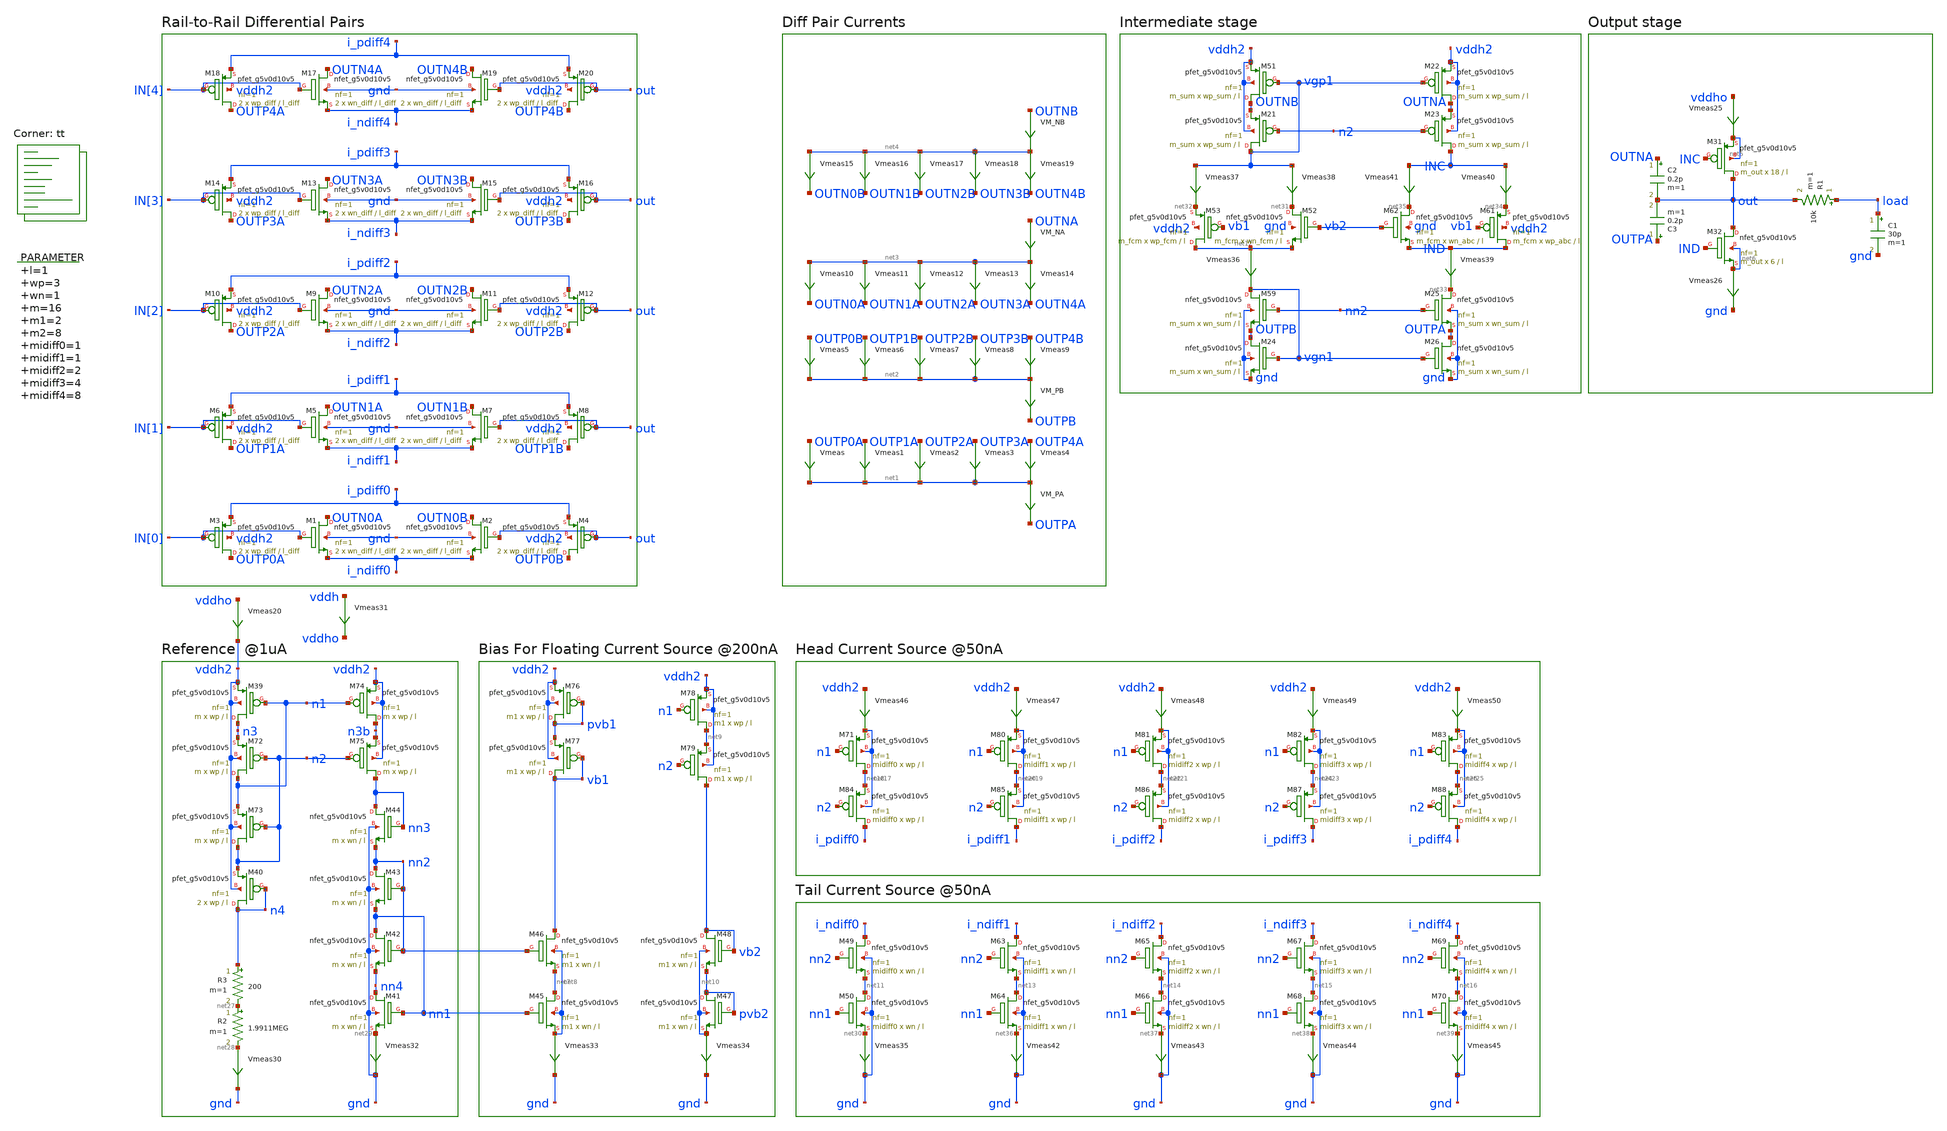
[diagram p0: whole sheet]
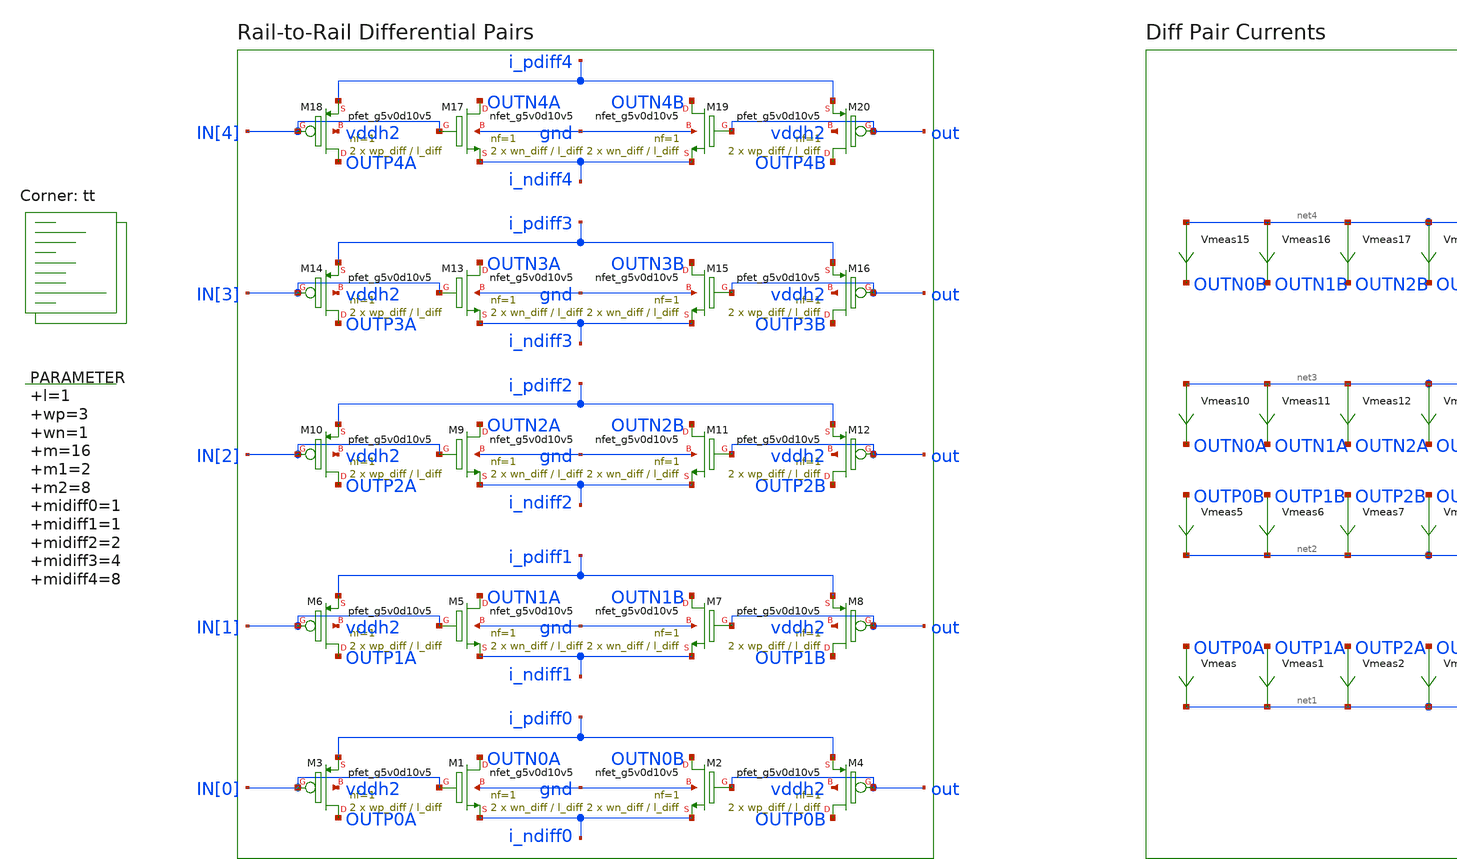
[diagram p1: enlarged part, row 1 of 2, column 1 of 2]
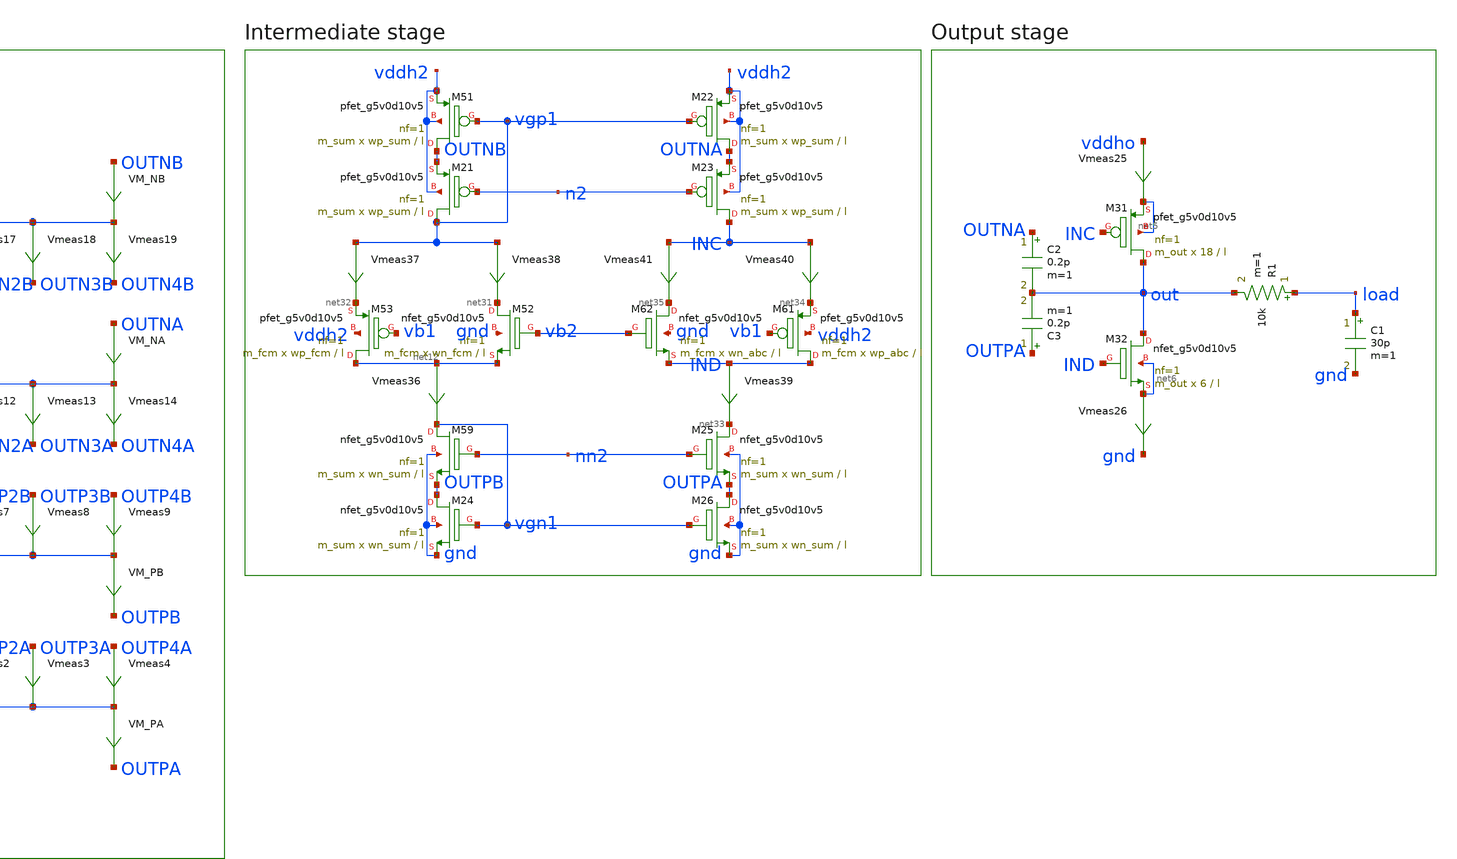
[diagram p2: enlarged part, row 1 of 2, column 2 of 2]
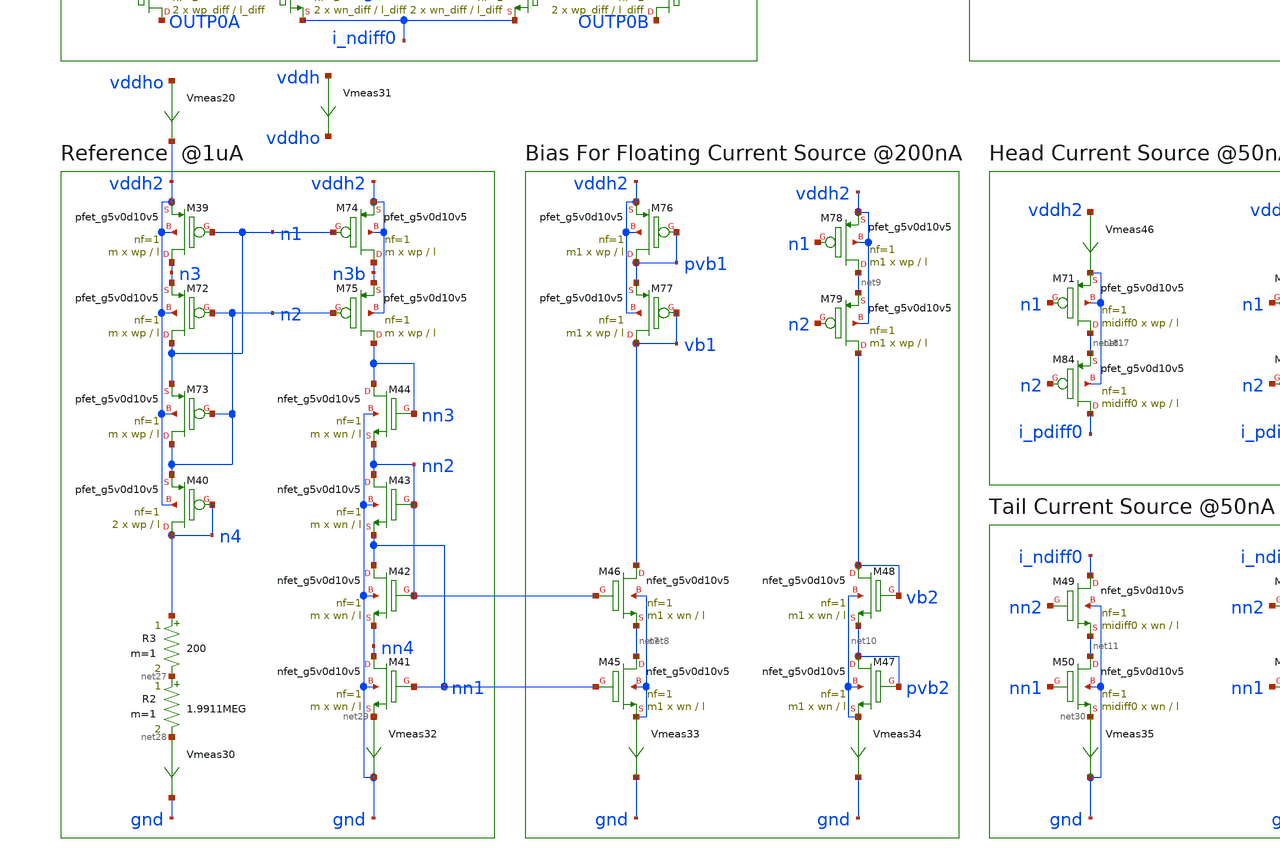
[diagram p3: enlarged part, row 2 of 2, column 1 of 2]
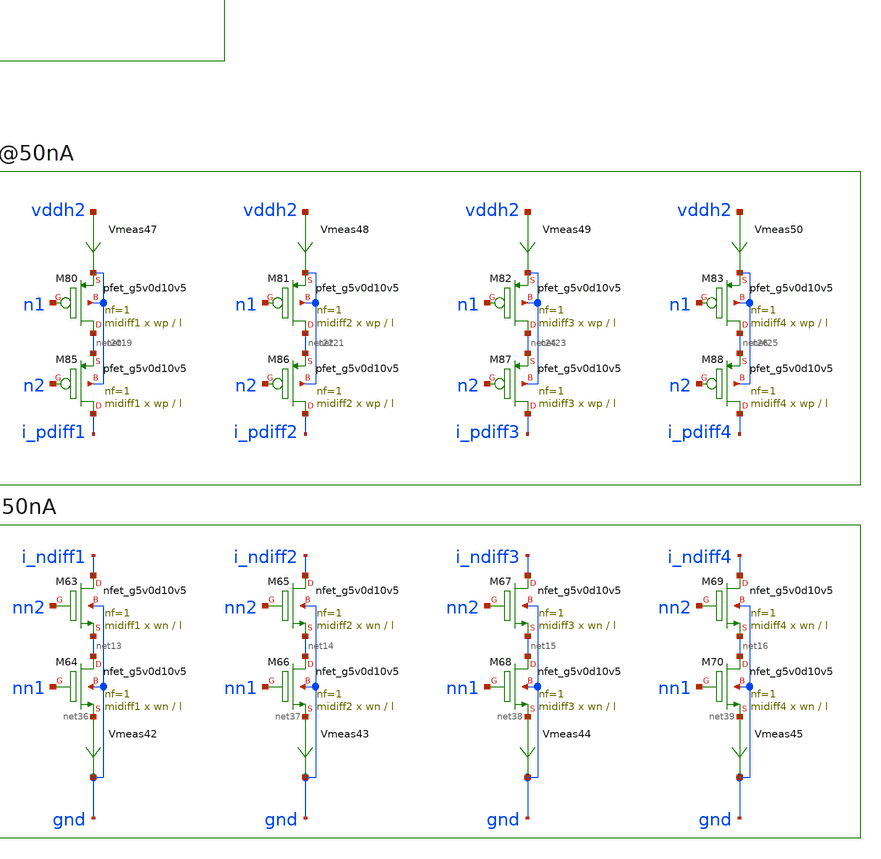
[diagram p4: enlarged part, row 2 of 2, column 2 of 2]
** sch_path: xschem/op_amp_v2-tb.sch
**.subckt op_amp_v2-tb
XM1 OUTN0A IN[0] i_ndiff0 gnd sky130_fd_pr__nfet_g5v0d10v5 L=l_diff W=wn_diff nf=1 ad='int((nf+1)/2) * W/nf * 0.29'
+ as='int((nf+2)/2) * W/nf * 0.29' pd='2*int((nf+1)/2) * (W/nf + 0.29)' ps='2*int((nf+2)/2) * (W/nf + 0.29)'
+ nrd='0.29 / W' nrs='0.29 / W' sa=0 sb=0 sd=0 mult=2 m=2
XM3 OUTP0A IN[0] i_pdiff0 vddh2 sky130_fd_pr__pfet_g5v0d10v5 L=l_diff W=wp_diff nf=1 ad='int((nf+1)/2) * W/nf * 0.29'
+ as='int((nf+2)/2) * W/nf * 0.29' pd='2*int((nf+1)/2) * (W/nf + 0.29)' ps='2*int((nf+2)/2) * (W/nf + 0.29)'
+ nrd='0.29 / W' nrs='0.29 / W' sa=0 sb=0 sd=0 mult=2 m=2
Vmeas OUTP0A net1 0
.save i(vmeas)
Vmeas1 OUTP1A net1 0
.save i(vmeas1)
Vmeas2 OUTP2A net1 0
.save i(vmeas2)
Vmeas3 OUTP3A net1 0
.save i(vmeas3)
Vmeas4 OUTP4A net1 0
.save i(vmeas4)
Vmeas5 OUTP0B net2 0
.save i(vmeas5)
Vmeas6 OUTP1B net2 0
.save i(vmeas6)
Vmeas7 OUTP2B net2 0
.save i(vmeas7)
Vmeas8 OUTP3B net2 0
.save i(vmeas8)
Vmeas9 OUTP4B net2 0
.save i(vmeas9)
Vmeas10 net3 OUTN0A 0
.save i(vmeas10)
Vmeas11 net3 OUTN1A 0
.save i(vmeas11)
Vmeas12 net3 OUTN2A 0
.save i(vmeas12)
Vmeas13 net3 OUTN3A 0
.save i(vmeas13)
Vmeas14 net3 OUTN4A 0
.save i(vmeas14)
Vmeas15 net4 OUTN0B 0
.save i(vmeas15)
Vmeas16 net4 OUTN1B 0
.save i(vmeas16)
Vmeas17 net4 OUTN2B 0
.save i(vmeas17)
Vmeas18 net4 OUTN3B 0
.save i(vmeas18)
Vmeas19 net4 OUTN4B 0
.save i(vmeas19)
XM31 out INC net5 net5 sky130_fd_pr__pfet_g5v0d10v5 L=l W=18 nf=1 ad='int((nf+1)/2) * W/nf * 0.29' as='int((nf+2)/2) * W/nf * 0.29'
+ pd='2*int((nf+1)/2) * (W/nf + 0.29)' ps='2*int((nf+2)/2) * (W/nf + 0.29)' nrd='0.29 / W' nrs='0.29 / W'
+ sa=0 sb=0 sd=0 mult=m_out m=m_out
XM32 out IND net6 net6 sky130_fd_pr__nfet_g5v0d10v5 L=l W=6 nf=1 ad='int((nf+1)/2) * W/nf * 0.29' as='int((nf+2)/2) * W/nf * 0.29'
+ pd='2*int((nf+1)/2) * (W/nf + 0.29)' ps='2*int((nf+2)/2) * (W/nf + 0.29)' nrd='0.29 / W' nrs='0.29 / W'
+ sa=0 sb=0 sd=0 mult=m_out m=m_out
R1 load out 10k m=1
Vmeas25 vddho net5 0
.save i(vmeas25)
Vmeas26 net6 gnd 0
.save i(vmeas26)
C1 load gnd 30p m=1
VM_NB OUTNB net4 0
.save i(vm_nb)
VM_NA OUTNA net3 0
.save i(vm_na)
VM_PB net2 OUTPB 0
.save i(vm_pb)
VM_PA net1 OUTPA 0
.save i(vm_pa)
C2 OUTNA out 0.2p m=1
C3 OUTPA out 0.2p m=1
XM2 OUTN0B out i_ndiff0 gnd sky130_fd_pr__nfet_g5v0d10v5 L=l_diff W=wn_diff nf=1 ad='int((nf+1)/2) * W/nf * 0.29'
+ as='int((nf+2)/2) * W/nf * 0.29' pd='2*int((nf+1)/2) * (W/nf + 0.29)' ps='2*int((nf+2)/2) * (W/nf + 0.29)'
+ nrd='0.29 / W' nrs='0.29 / W' sa=0 sb=0 sd=0 mult=2 m=2
XM4 OUTP0B out i_pdiff0 vddh2 sky130_fd_pr__pfet_g5v0d10v5 L=l_diff W=wp_diff nf=1 ad='int((nf+1)/2) * W/nf * 0.29'
+ as='int((nf+2)/2) * W/nf * 0.29' pd='2*int((nf+1)/2) * (W/nf + 0.29)' ps='2*int((nf+2)/2) * (W/nf + 0.29)'
+ nrd='0.29 / W' nrs='0.29 / W' sa=0 sb=0 sd=0 mult=2 m=2
XM5 OUTN1A IN[1] i_ndiff1 gnd sky130_fd_pr__nfet_g5v0d10v5 L=l_diff W=wn_diff nf=1 ad='int((nf+1)/2) * W/nf * 0.29'
+ as='int((nf+2)/2) * W/nf * 0.29' pd='2*int((nf+1)/2) * (W/nf + 0.29)' ps='2*int((nf+2)/2) * (W/nf + 0.29)'
+ nrd='0.29 / W' nrs='0.29 / W' sa=0 sb=0 sd=0 mult=2 m=2
XM6 OUTP1A IN[1] i_pdiff1 vddh2 sky130_fd_pr__pfet_g5v0d10v5 L=l_diff W=wp_diff nf=1 ad='int((nf+1)/2) * W/nf * 0.29'
+ as='int((nf+2)/2) * W/nf * 0.29' pd='2*int((nf+1)/2) * (W/nf + 0.29)' ps='2*int((nf+2)/2) * (W/nf + 0.29)'
+ nrd='0.29 / W' nrs='0.29 / W' sa=0 sb=0 sd=0 mult=2 m=2
XM7 OUTN1B out i_ndiff1 gnd sky130_fd_pr__nfet_g5v0d10v5 L=l_diff W=wn_diff nf=1 ad='int((nf+1)/2) * W/nf * 0.29'
+ as='int((nf+2)/2) * W/nf * 0.29' pd='2*int((nf+1)/2) * (W/nf + 0.29)' ps='2*int((nf+2)/2) * (W/nf + 0.29)'
+ nrd='0.29 / W' nrs='0.29 / W' sa=0 sb=0 sd=0 mult=2 m=2
XM8 OUTP1B out i_pdiff1 vddh2 sky130_fd_pr__pfet_g5v0d10v5 L=l_diff W=wp_diff nf=1 ad='int((nf+1)/2) * W/nf * 0.29'
+ as='int((nf+2)/2) * W/nf * 0.29' pd='2*int((nf+1)/2) * (W/nf + 0.29)' ps='2*int((nf+2)/2) * (W/nf + 0.29)'
+ nrd='0.29 / W' nrs='0.29 / W' sa=0 sb=0 sd=0 mult=2 m=2
XM9 OUTN2A IN[2] i_ndiff2 gnd sky130_fd_pr__nfet_g5v0d10v5 L=l_diff W=wn_diff nf=1 ad='int((nf+1)/2) * W/nf * 0.29'
+ as='int((nf+2)/2) * W/nf * 0.29' pd='2*int((nf+1)/2) * (W/nf + 0.29)' ps='2*int((nf+2)/2) * (W/nf + 0.29)'
+ nrd='0.29 / W' nrs='0.29 / W' sa=0 sb=0 sd=0 mult=2 m=2
XM10 OUTP2A IN[2] i_pdiff2 vddh2 sky130_fd_pr__pfet_g5v0d10v5 L=l_diff W=wp_diff nf=1 ad='int((nf+1)/2) * W/nf * 0.29'
+ as='int((nf+2)/2) * W/nf * 0.29' pd='2*int((nf+1)/2) * (W/nf + 0.29)' ps='2*int((nf+2)/2) * (W/nf + 0.29)'
+ nrd='0.29 / W' nrs='0.29 / W' sa=0 sb=0 sd=0 mult=2 m=2
XM11 OUTN2B out i_ndiff2 gnd sky130_fd_pr__nfet_g5v0d10v5 L=l_diff W=wn_diff nf=1 ad='int((nf+1)/2) * W/nf * 0.29'
+ as='int((nf+2)/2) * W/nf * 0.29' pd='2*int((nf+1)/2) * (W/nf + 0.29)' ps='2*int((nf+2)/2) * (W/nf + 0.29)'
+ nrd='0.29 / W' nrs='0.29 / W' sa=0 sb=0 sd=0 mult=2 m=2
XM12 OUTP2B out i_pdiff2 vddh2 sky130_fd_pr__pfet_g5v0d10v5 L=l_diff W=wp_diff nf=1 ad='int((nf+1)/2) * W/nf * 0.29'
+ as='int((nf+2)/2) * W/nf * 0.29' pd='2*int((nf+1)/2) * (W/nf + 0.29)' ps='2*int((nf+2)/2) * (W/nf + 0.29)'
+ nrd='0.29 / W' nrs='0.29 / W' sa=0 sb=0 sd=0 mult=2 m=2
XM13 OUTN3A IN[3] i_ndiff3 gnd sky130_fd_pr__nfet_g5v0d10v5 L=l_diff W=wn_diff nf=1 ad='int((nf+1)/2) * W/nf * 0.29'
+ as='int((nf+2)/2) * W/nf * 0.29' pd='2*int((nf+1)/2) * (W/nf + 0.29)' ps='2*int((nf+2)/2) * (W/nf + 0.29)'
+ nrd='0.29 / W' nrs='0.29 / W' sa=0 sb=0 sd=0 mult=2 m=2
XM14 OUTP3A IN[3] i_pdiff3 vddh2 sky130_fd_pr__pfet_g5v0d10v5 L=l_diff W=wp_diff nf=1 ad='int((nf+1)/2) * W/nf * 0.29'
+ as='int((nf+2)/2) * W/nf * 0.29' pd='2*int((nf+1)/2) * (W/nf + 0.29)' ps='2*int((nf+2)/2) * (W/nf + 0.29)'
+ nrd='0.29 / W' nrs='0.29 / W' sa=0 sb=0 sd=0 mult=2 m=2
XM15 OUTN3B out i_ndiff3 gnd sky130_fd_pr__nfet_g5v0d10v5 L=l_diff W=wn_diff nf=1 ad='int((nf+1)/2) * W/nf * 0.29'
+ as='int((nf+2)/2) * W/nf * 0.29' pd='2*int((nf+1)/2) * (W/nf + 0.29)' ps='2*int((nf+2)/2) * (W/nf + 0.29)'
+ nrd='0.29 / W' nrs='0.29 / W' sa=0 sb=0 sd=0 mult=2 m=2
XM16 OUTP3B out i_pdiff3 vddh2 sky130_fd_pr__pfet_g5v0d10v5 L=l_diff W=wp_diff nf=1 ad='int((nf+1)/2) * W/nf * 0.29'
+ as='int((nf+2)/2) * W/nf * 0.29' pd='2*int((nf+1)/2) * (W/nf + 0.29)' ps='2*int((nf+2)/2) * (W/nf + 0.29)'
+ nrd='0.29 / W' nrs='0.29 / W' sa=0 sb=0 sd=0 mult=2 m=2
XM17 OUTN4A IN[4] i_ndiff4 gnd sky130_fd_pr__nfet_g5v0d10v5 L=l_diff W=wn_diff nf=1 ad='int((nf+1)/2) * W/nf * 0.29'
+ as='int((nf+2)/2) * W/nf * 0.29' pd='2*int((nf+1)/2) * (W/nf + 0.29)' ps='2*int((nf+2)/2) * (W/nf + 0.29)'
+ nrd='0.29 / W' nrs='0.29 / W' sa=0 sb=0 sd=0 mult=2 m=2
XM18 OUTP4A IN[4] i_pdiff4 vddh2 sky130_fd_pr__pfet_g5v0d10v5 L=l_diff W=wp_diff nf=1 ad='int((nf+1)/2) * W/nf * 0.29'
+ as='int((nf+2)/2) * W/nf * 0.29' pd='2*int((nf+1)/2) * (W/nf + 0.29)' ps='2*int((nf+2)/2) * (W/nf + 0.29)'
+ nrd='0.29 / W' nrs='0.29 / W' sa=0 sb=0 sd=0 mult=2 m=2
XM19 OUTN4B out i_ndiff4 gnd sky130_fd_pr__nfet_g5v0d10v5 L=l_diff W=wn_diff nf=1 ad='int((nf+1)/2) * W/nf * 0.29'
+ as='int((nf+2)/2) * W/nf * 0.29' pd='2*int((nf+1)/2) * (W/nf + 0.29)' ps='2*int((nf+2)/2) * (W/nf + 0.29)'
+ nrd='0.29 / W' nrs='0.29 / W' sa=0 sb=0 sd=0 mult=2 m=2
XM20 OUTP4B out i_pdiff4 vddh2 sky130_fd_pr__pfet_g5v0d10v5 L=l_diff W=wp_diff nf=1 ad='int((nf+1)/2) * W/nf * 0.29'
+ as='int((nf+2)/2) * W/nf * 0.29' pd='2*int((nf+1)/2) * (W/nf + 0.29)' ps='2*int((nf+2)/2) * (W/nf + 0.29)'
+ nrd='0.29 / W' nrs='0.29 / W' sa=0 sb=0 sd=0 mult=2 m=2
XM39 n3 n1 vddh2 vddh2 sky130_fd_pr__pfet_g5v0d10v5 L=l W=wp nf=1 ad='int((nf+1)/2) * W/nf * 0.29' as='int((nf+2)/2) * W/nf * 0.29'
+ pd='2*int((nf+1)/2) * (W/nf + 0.29)' ps='2*int((nf+2)/2) * (W/nf + 0.29)' nrd='0.29 / W' nrs='0.29 / W'
+ sa=0 sb=0 sd=0 mult=m m=m
R2 net27 net28 1.9911MEG m=1
Vmeas30 net28 gnd 0
.save i(vmeas30)
R3 n4 net27 200 m=1
XM40 n4 n4 n2 vddh2 sky130_fd_pr__pfet_g5v0d10v5 L=l W=wp nf=1 ad='int((nf+1)/2) * W/nf * 0.29' as='int((nf+2)/2) * W/nf * 0.29'
+ pd='2*int((nf+1)/2) * (W/nf + 0.29)' ps='2*int((nf+2)/2) * (W/nf + 0.29)' nrd='0.29 / W' nrs='0.29 / W'
+ sa=0 sb=0 sd=0 mult=2 m=2
Vmeas31 vddh vddho 0
.save i(vmeas31)
XM41 nn4 nn1 net29 gnd sky130_fd_pr__nfet_g5v0d10v5 L=l W=wn nf=1 ad='int((nf+1)/2) * W/nf * 0.29' as='int((nf+2)/2) * W/nf * 0.29'
+ pd='2*int((nf+1)/2) * (W/nf + 0.29)' ps='2*int((nf+2)/2) * (W/nf + 0.29)' nrd='0.29 / W' nrs='0.29 / W'
+ sa=0 sb=0 sd=0 mult=m m=m
XM42 nn1 nn2 nn4 gnd sky130_fd_pr__nfet_g5v0d10v5 L=l W=wn nf=1 ad='int((nf+1)/2) * W/nf * 0.29' as='int((nf+2)/2) * W/nf * 0.29'
+ pd='2*int((nf+1)/2) * (W/nf + 0.29)' ps='2*int((nf+2)/2) * (W/nf + 0.29)' nrd='0.29 / W' nrs='0.29 / W'
+ sa=0 sb=0 sd=0 mult=m m=m
XM43 nn2 nn2 nn1 gnd sky130_fd_pr__nfet_g5v0d10v5 L=l W=wn nf=1 ad='int((nf+1)/2) * W/nf * 0.29' as='int((nf+2)/2) * W/nf * 0.29'
+ pd='2*int((nf+1)/2) * (W/nf + 0.29)' ps='2*int((nf+2)/2) * (W/nf + 0.29)' nrd='0.29 / W' nrs='0.29 / W'
+ sa=0 sb=0 sd=0 mult=m m=m
XM44 nn3 nn3 nn2 gnd sky130_fd_pr__nfet_g5v0d10v5 L=l W=wn nf=1 ad='int((nf+1)/2) * W/nf * 0.29' as='int((nf+2)/2) * W/nf * 0.29'
+ pd='2*int((nf+1)/2) * (W/nf + 0.29)' ps='2*int((nf+2)/2) * (W/nf + 0.29)' nrd='0.29 / W' nrs='0.29 / W'
+ sa=0 sb=0 sd=0 mult=m m=m
Vmeas32 net29 gnd 0
.save i(vmeas32)
XM45 net7 nn1 net8 net8 sky130_fd_pr__nfet_g5v0d10v5 L=l W=wn nf=1 ad='int((nf+1)/2) * W/nf * 0.29' as='int((nf+2)/2) * W/nf * 0.29'
+ pd='2*int((nf+1)/2) * (W/nf + 0.29)' ps='2*int((nf+2)/2) * (W/nf + 0.29)' nrd='0.29 / W' nrs='0.29 / W'
+ sa=0 sb=0 sd=0 mult=m1 m=m1
XM46 vb1 nn2 net7 net8 sky130_fd_pr__nfet_g5v0d10v5 L=l W=wn nf=1 ad='int((nf+1)/2) * W/nf * 0.29' as='int((nf+2)/2) * W/nf * 0.29'
+ pd='2*int((nf+1)/2) * (W/nf + 0.29)' ps='2*int((nf+2)/2) * (W/nf + 0.29)' nrd='0.29 / W' nrs='0.29 / W'
+ sa=0 sb=0 sd=0 mult=m1 m=m1
Vmeas33 net8 gnd 0
.save i(vmeas33)
XM47 pvb2 pvb2 net10 net10 sky130_fd_pr__nfet_g5v0d10v5 L=l W=wn nf=1 ad='int((nf+1)/2) * W/nf * 0.29'
+ as='int((nf+2)/2) * W/nf * 0.29' pd='2*int((nf+1)/2) * (W/nf + 0.29)' ps='2*int((nf+2)/2) * (W/nf + 0.29)'
+ nrd='0.29 / W' nrs='0.29 / W' sa=0 sb=0 sd=0 mult=m1 m=m1
XM48 vb2 vb2 pvb2 net10 sky130_fd_pr__nfet_g5v0d10v5 L=l W=wn nf=1 ad='int((nf+1)/2) * W/nf * 0.29' as='int((nf+2)/2) * W/nf * 0.29'
+ pd='2*int((nf+1)/2) * (W/nf + 0.29)' ps='2*int((nf+2)/2) * (W/nf + 0.29)' nrd='0.29 / W' nrs='0.29 / W'
+ sa=0 sb=0 sd=0 mult=m1 m=m1
Vmeas34 net10 gnd 0
.save i(vmeas34)
XM49 i_ndiff0 nn2 net11 gnd sky130_fd_pr__nfet_g5v0d10v5 L=l W=wn nf=1 ad='int((nf+1)/2) * W/nf * 0.29'
+ as='int((nf+2)/2) * W/nf * 0.29' pd='2*int((nf+1)/2) * (W/nf + 0.29)' ps='2*int((nf+2)/2) * (W/nf + 0.29)'
+ nrd='0.29 / W' nrs='0.29 / W' sa=0 sb=0 sd=0 mult=midiff0 m=midiff0
XM50 net11 nn1 net30 gnd sky130_fd_pr__nfet_g5v0d10v5 L=l W=wn nf=1 ad='int((nf+1)/2) * W/nf * 0.29'
+ as='int((nf+2)/2) * W/nf * 0.29' pd='2*int((nf+1)/2) * (W/nf + 0.29)' ps='2*int((nf+2)/2) * (W/nf + 0.29)'
+ nrd='0.29 / W' nrs='0.29 / W' sa=0 sb=0 sd=0 mult=midiff0 m=midiff0
Vmeas35 net30 gnd 0
.save i(vmeas35)
Vmeas36 net12 vgn1 0
.save i(vmeas36)
XM51 OUTNB vgp1 vddh2 vddh2 sky130_fd_pr__pfet_g5v0d10v5 L=l W=wp_sum nf=1 ad='int((nf+1)/2) * W/nf * 0.29'
+ as='int((nf+2)/2) * W/nf * 0.29' pd='2*int((nf+1)/2) * (W/nf + 0.29)' ps='2*int((nf+2)/2) * (W/nf + 0.29)'
+ nrd='0.29 / W' nrs='0.29 / W' sa=0 sb=0 sd=0 mult=m_sum m=m_sum
XM52 net31 vb2 net12 gnd sky130_fd_pr__nfet_g5v0d10v5 L=l W=wn_fcm nf=1 ad='int((nf+1)/2) * W/nf * 0.29'
+ as='int((nf+2)/2) * W/nf * 0.29' pd='2*int((nf+1)/2) * (W/nf + 0.29)' ps='2*int((nf+2)/2) * (W/nf + 0.29)'
+ nrd='0.29 / W' nrs='0.29 / W' sa=0 sb=0 sd=0 mult=m_fcm m=m_fcm
Vmeas37 vgp1 net32 0
.save i(vmeas37)
Vmeas38 vgp1 net31 0
.save i(vmeas38)
XM53 net12 vb1 net32 vddh2 sky130_fd_pr__pfet_g5v0d10v5 L=l W=wp_fcm nf=1 ad='int((nf+1)/2) * W/nf * 0.29'
+ as='int((nf+2)/2) * W/nf * 0.29' pd='2*int((nf+1)/2) * (W/nf + 0.29)' ps='2*int((nf+2)/2) * (W/nf + 0.29)'
+ nrd='0.29 / W' nrs='0.29 / W' sa=0 sb=0 sd=0 mult=m_fcm m=m_fcm
Vmeas39 IND net33 0
.save i(vmeas39)
Vmeas40 INC net34 0
.save i(vmeas40)
Vmeas41 INC net35 0
.save i(vmeas41)
XM59 vgn1 nn2 OUTPB gnd sky130_fd_pr__nfet_g5v0d10v5 L=l W=wn_sum nf=1 ad='int((nf+1)/2) * W/nf * 0.29'
+ as='int((nf+2)/2) * W/nf * 0.29' pd='2*int((nf+1)/2) * (W/nf + 0.29)' ps='2*int((nf+2)/2) * (W/nf + 0.29)'
+ nrd='0.29 / W' nrs='0.29 / W' sa=0 sb=0 sd=0 mult=m_sum m=m_sum
XM61 IND vb1 net34 vddh2 sky130_fd_pr__pfet_g5v0d10v5 L=l W=wp_abc nf=1 ad='int((nf+1)/2) * W/nf * 0.29'
+ as='int((nf+2)/2) * W/nf * 0.29' pd='2*int((nf+1)/2) * (W/nf + 0.29)' ps='2*int((nf+2)/2) * (W/nf + 0.29)'
+ nrd='0.29 / W' nrs='0.29 / W' sa=0 sb=0 sd=0 mult=m_fcm m=m_fcm
XM62 net35 vb2 IND gnd sky130_fd_pr__nfet_g5v0d10v5 L=l W=wn_abc nf=1 ad='int((nf+1)/2) * W/nf * 0.29'
+ as='int((nf+2)/2) * W/nf * 0.29' pd='2*int((nf+1)/2) * (W/nf + 0.29)' ps='2*int((nf+2)/2) * (W/nf + 0.29)'
+ nrd='0.29 / W' nrs='0.29 / W' sa=0 sb=0 sd=0 mult=m_fcm m=m_fcm
XM63 i_ndiff1 nn2 net13 gnd sky130_fd_pr__nfet_g5v0d10v5 L=l W=wn nf=1 ad='int((nf+1)/2) * W/nf * 0.29'
+ as='int((nf+2)/2) * W/nf * 0.29' pd='2*int((nf+1)/2) * (W/nf + 0.29)' ps='2*int((nf+2)/2) * (W/nf + 0.29)'
+ nrd='0.29 / W' nrs='0.29 / W' sa=0 sb=0 sd=0 mult=midiff1 m=midiff1
XM64 net13 nn1 net36 gnd sky130_fd_pr__nfet_g5v0d10v5 L=l W=wn nf=1 ad='int((nf+1)/2) * W/nf * 0.29'
+ as='int((nf+2)/2) * W/nf * 0.29' pd='2*int((nf+1)/2) * (W/nf + 0.29)' ps='2*int((nf+2)/2) * (W/nf + 0.29)'
+ nrd='0.29 / W' nrs='0.29 / W' sa=0 sb=0 sd=0 mult=midiff1 m=midiff1
Vmeas42 net36 gnd 0
.save i(vmeas42)
XM65 i_ndiff2 nn2 net14 gnd sky130_fd_pr__nfet_g5v0d10v5 L=l W=wn nf=1 ad='int((nf+1)/2) * W/nf * 0.29'
+ as='int((nf+2)/2) * W/nf * 0.29' pd='2*int((nf+1)/2) * (W/nf + 0.29)' ps='2*int((nf+2)/2) * (W/nf + 0.29)'
+ nrd='0.29 / W' nrs='0.29 / W' sa=0 sb=0 sd=0 mult=midiff2 m=midiff2
XM66 net14 nn1 net37 gnd sky130_fd_pr__nfet_g5v0d10v5 L=l W=wn nf=1 ad='int((nf+1)/2) * W/nf * 0.29'
+ as='int((nf+2)/2) * W/nf * 0.29' pd='2*int((nf+1)/2) * (W/nf + 0.29)' ps='2*int((nf+2)/2) * (W/nf + 0.29)'
+ nrd='0.29 / W' nrs='0.29 / W' sa=0 sb=0 sd=0 mult=midiff2 m=midiff2
Vmeas43 net37 gnd 0
.save i(vmeas43)
XM67 i_ndiff3 nn2 net15 gnd sky130_fd_pr__nfet_g5v0d10v5 L=l W=wn nf=1 ad='int((nf+1)/2) * W/nf * 0.29'
+ as='int((nf+2)/2) * W/nf * 0.29' pd='2*int((nf+1)/2) * (W/nf + 0.29)' ps='2*int((nf+2)/2) * (W/nf + 0.29)'
+ nrd='0.29 / W' nrs='0.29 / W' sa=0 sb=0 sd=0 mult=midiff3 m=midiff3
XM68 net15 nn1 net38 gnd sky130_fd_pr__nfet_g5v0d10v5 L=l W=wn nf=1 ad='int((nf+1)/2) * W/nf * 0.29'
+ as='int((nf+2)/2) * W/nf * 0.29' pd='2*int((nf+1)/2) * (W/nf + 0.29)' ps='2*int((nf+2)/2) * (W/nf + 0.29)'
+ nrd='0.29 / W' nrs='0.29 / W' sa=0 sb=0 sd=0 mult=midiff3 m=midiff3
Vmeas44 net38 gnd 0
.save i(vmeas44)
XM69 i_ndiff4 nn2 net16 gnd sky130_fd_pr__nfet_g5v0d10v5 L=l W=wn nf=1 ad='int((nf+1)/2) * W/nf * 0.29'
+ as='int((nf+2)/2) * W/nf * 0.29' pd='2*int((nf+1)/2) * (W/nf + 0.29)' ps='2*int((nf+2)/2) * (W/nf + 0.29)'
+ nrd='0.29 / W' nrs='0.29 / W' sa=0 sb=0 sd=0 mult=midiff4 m=midiff4
XM70 net16 nn1 net39 gnd sky130_fd_pr__nfet_g5v0d10v5 L=l W=wn nf=1 ad='int((nf+1)/2) * W/nf * 0.29'
+ as='int((nf+2)/2) * W/nf * 0.29' pd='2*int((nf+1)/2) * (W/nf + 0.29)' ps='2*int((nf+2)/2) * (W/nf + 0.29)'
+ nrd='0.29 / W' nrs='0.29 / W' sa=0 sb=0 sd=0 mult=midiff4 m=midiff4
Vmeas45 net39 gnd 0
.save i(vmeas45)
XM71 net18 n1 net17 net17 sky130_fd_pr__pfet_g5v0d10v5 L=l W=wp nf=1 ad='int((nf+1)/2) * W/nf * 0.29'
+ as='int((nf+2)/2) * W/nf * 0.29' pd='2*int((nf+1)/2) * (W/nf + 0.29)' ps='2*int((nf+2)/2) * (W/nf + 0.29)'
+ nrd='0.29 / W' nrs='0.29 / W' sa=0 sb=0 sd=0 mult=midiff0 m=midiff0
Vmeas46 vddh2 net17 0
.save i(vmeas46)
XM72 n1 n2 n3 vddh2 sky130_fd_pr__pfet_g5v0d10v5 L=l W=wp nf=1 ad='int((nf+1)/2) * W/nf * 0.29' as='int((nf+2)/2) * W/nf * 0.29'
+ pd='2*int((nf+1)/2) * (W/nf + 0.29)' ps='2*int((nf+2)/2) * (W/nf + 0.29)' nrd='0.29 / W' nrs='0.29 / W'
+ sa=0 sb=0 sd=0 mult=m m=m
XM73 n2 n2 n1 vddh2 sky130_fd_pr__pfet_g5v0d10v5 L=l W=wp nf=1 ad='int((nf+1)/2) * W/nf * 0.29' as='int((nf+2)/2) * W/nf * 0.29'
+ pd='2*int((nf+1)/2) * (W/nf + 0.29)' ps='2*int((nf+2)/2) * (W/nf + 0.29)' nrd='0.29 / W' nrs='0.29 / W'
+ sa=0 sb=0 sd=0 mult=m m=m
XM74 n3b n1 vddh2 vddh2 sky130_fd_pr__pfet_g5v0d10v5 L=l W=wp nf=1 ad='int((nf+1)/2) * W/nf * 0.29' as='int((nf+2)/2) * W/nf * 0.29'
+ pd='2*int((nf+1)/2) * (W/nf + 0.29)' ps='2*int((nf+2)/2) * (W/nf + 0.29)' nrd='0.29 / W' nrs='0.29 / W'
+ sa=0 sb=0 sd=0 mult=m m=m
XM75 nn3 n2 n3b vddh2 sky130_fd_pr__pfet_g5v0d10v5 L=l W=wp nf=1 ad='int((nf+1)/2) * W/nf * 0.29' as='int((nf+2)/2) * W/nf * 0.29'
+ pd='2*int((nf+1)/2) * (W/nf + 0.29)' ps='2*int((nf+2)/2) * (W/nf + 0.29)' nrd='0.29 / W' nrs='0.29 / W'
+ sa=0 sb=0 sd=0 mult=m m=m
XM76 pvb1 pvb1 vddh2 vddh2 sky130_fd_pr__pfet_g5v0d10v5 L=l W=wp nf=1 ad='int((nf+1)/2) * W/nf * 0.29'
+ as='int((nf+2)/2) * W/nf * 0.29' pd='2*int((nf+1)/2) * (W/nf + 0.29)' ps='2*int((nf+2)/2) * (W/nf + 0.29)'
+ nrd='0.29 / W' nrs='0.29 / W' sa=0 sb=0 sd=0 mult=m1 m=m1
XM77 vb1 vb1 pvb1 vddh2 sky130_fd_pr__pfet_g5v0d10v5 L=l W=wp nf=1 ad='int((nf+1)/2) * W/nf * 0.29' as='int((nf+2)/2) * W/nf * 0.29'
+ pd='2*int((nf+1)/2) * (W/nf + 0.29)' ps='2*int((nf+2)/2) * (W/nf + 0.29)' nrd='0.29 / W' nrs='0.29 / W'
+ sa=0 sb=0 sd=0 mult=m1 m=m1
XM78 net9 n1 vddh2 vddh2 sky130_fd_pr__pfet_g5v0d10v5 L=l W=wp nf=1 ad='int((nf+1)/2) * W/nf * 0.29'
+ as='int((nf+2)/2) * W/nf * 0.29' pd='2*int((nf+1)/2) * (W/nf + 0.29)' ps='2*int((nf+2)/2) * (W/nf + 0.29)'
+ nrd='0.29 / W' nrs='0.29 / W' sa=0 sb=0 sd=0 mult=m1 m=m1
XM79 vb2 n2 net9 vddh2 sky130_fd_pr__pfet_g5v0d10v5 L=l W=wp nf=1 ad='int((nf+1)/2) * W/nf * 0.29' as='int((nf+2)/2) * W/nf * 0.29'
+ pd='2*int((nf+1)/2) * (W/nf + 0.29)' ps='2*int((nf+2)/2) * (W/nf + 0.29)' nrd='0.29 / W' nrs='0.29 / W'
+ sa=0 sb=0 sd=0 mult=m1 m=m1
XM80 net20 n1 net19 net19 sky130_fd_pr__pfet_g5v0d10v5 L=l W=wp nf=1 ad='int((nf+1)/2) * W/nf * 0.29'
+ as='int((nf+2)/2) * W/nf * 0.29' pd='2*int((nf+1)/2) * (W/nf + 0.29)' ps='2*int((nf+2)/2) * (W/nf + 0.29)'
+ nrd='0.29 / W' nrs='0.29 / W' sa=0 sb=0 sd=0 mult=midiff1 m=midiff1
Vmeas47 vddh2 net19 0
.save i(vmeas47)
XM81 net22 n1 net21 net21 sky130_fd_pr__pfet_g5v0d10v5 L=l W=wp nf=1 ad='int((nf+1)/2) * W/nf * 0.29'
+ as='int((nf+2)/2) * W/nf * 0.29' pd='2*int((nf+1)/2) * (W/nf + 0.29)' ps='2*int((nf+2)/2) * (W/nf + 0.29)'
+ nrd='0.29 / W' nrs='0.29 / W' sa=0 sb=0 sd=0 mult=midiff2 m=midiff2
Vmeas48 vddh2 net21 0
.save i(vmeas48)
XM82 net24 n1 net23 net23 sky130_fd_pr__pfet_g5v0d10v5 L=l W=wp nf=1 ad='int((nf+1)/2) * W/nf * 0.29'
+ as='int((nf+2)/2) * W/nf * 0.29' pd='2*int((nf+1)/2) * (W/nf + 0.29)' ps='2*int((nf+2)/2) * (W/nf + 0.29)'
+ nrd='0.29 / W' nrs='0.29 / W' sa=0 sb=0 sd=0 mult=midiff3 m=midiff3
Vmeas49 vddh2 net23 0
.save i(vmeas49)
XM83 net26 n1 net25 net25 sky130_fd_pr__pfet_g5v0d10v5 L=l W=wp nf=1 ad='int((nf+1)/2) * W/nf * 0.29'
+ as='int((nf+2)/2) * W/nf * 0.29' pd='2*int((nf+1)/2) * (W/nf + 0.29)' ps='2*int((nf+2)/2) * (W/nf + 0.29)'
+ nrd='0.29 / W' nrs='0.29 / W' sa=0 sb=0 sd=0 mult=midiff4 m=midiff4
Vmeas50 vddh2 net25 0
.save i(vmeas50)
XM84 i_pdiff0 n2 net18 net17 sky130_fd_pr__pfet_g5v0d10v5 L=l W=wp nf=1 ad='int((nf+1)/2) * W/nf * 0.29'
+ as='int((nf+2)/2) * W/nf * 0.29' pd='2*int((nf+1)/2) * (W/nf + 0.29)' ps='2*int((nf+2)/2) * (W/nf + 0.29)'
+ nrd='0.29 / W' nrs='0.29 / W' sa=0 sb=0 sd=0 mult=midiff0 m=midiff0
XM85 i_pdiff1 n2 net20 net19 sky130_fd_pr__pfet_g5v0d10v5 L=l W=wp nf=1 ad='int((nf+1)/2) * W/nf * 0.29'
+ as='int((nf+2)/2) * W/nf * 0.29' pd='2*int((nf+1)/2) * (W/nf + 0.29)' ps='2*int((nf+2)/2) * (W/nf + 0.29)'
+ nrd='0.29 / W' nrs='0.29 / W' sa=0 sb=0 sd=0 mult=midiff1 m=midiff1
XM86 i_pdiff2 n2 net22 net21 sky130_fd_pr__pfet_g5v0d10v5 L=l W=wp nf=1 ad='int((nf+1)/2) * W/nf * 0.29'
+ as='int((nf+2)/2) * W/nf * 0.29' pd='2*int((nf+1)/2) * (W/nf + 0.29)' ps='2*int((nf+2)/2) * (W/nf + 0.29)'
+ nrd='0.29 / W' nrs='0.29 / W' sa=0 sb=0 sd=0 mult=midiff2 m=midiff2
XM87 i_pdiff3 n2 net24 net23 sky130_fd_pr__pfet_g5v0d10v5 L=l W=wp nf=1 ad='int((nf+1)/2) * W/nf * 0.29'
+ as='int((nf+2)/2) * W/nf * 0.29' pd='2*int((nf+1)/2) * (W/nf + 0.29)' ps='2*int((nf+2)/2) * (W/nf + 0.29)'
+ nrd='0.29 / W' nrs='0.29 / W' sa=0 sb=0 sd=0 mult=midiff3 m=midiff3
XM88 i_pdiff4 n2 net26 net25 sky130_fd_pr__pfet_g5v0d10v5 L=l W=wp nf=1 ad='int((nf+1)/2) * W/nf * 0.29'
+ as='int((nf+2)/2) * W/nf * 0.29' pd='2*int((nf+1)/2) * (W/nf + 0.29)' ps='2*int((nf+2)/2) * (W/nf + 0.29)'
+ nrd='0.29 / W' nrs='0.29 / W' sa=0 sb=0 sd=0 mult=midiff4 m=midiff4
.param l=1 wp=3 wn=1 m=16 m1=2 m2=8 midiff0=1 midiff1=1 midiff2=2 midiff3=4 midiff4=8 m_sum=2
+ m_fcm=2 wp_diff=3 wn_diff=1 l_diff=1 mdiff=2 m_out=2 wp_sum=15 wn_sum=5 wp_fcm=6 wn_fcm=2 wp_abc=6 wn_abc=2
XM21 vgp1 n2 OUTNB vddh2 sky130_fd_pr__pfet_g5v0d10v5 L=l W=wp_sum nf=1 ad='int((nf+1)/2) * W/nf * 0.29'
+ as='int((nf+2)/2) * W/nf * 0.29' pd='2*int((nf+1)/2) * (W/nf + 0.29)' ps='2*int((nf+2)/2) * (W/nf + 0.29)'
+ nrd='0.29 / W' nrs='0.29 / W' sa=0 sb=0 sd=0 mult=m_sum m=m_sum
XM22 OUTNA vgp1 vddh2 vddh2 sky130_fd_pr__pfet_g5v0d10v5 L=l W=wp_sum nf=1 ad='int((nf+1)/2) * W/nf * 0.29'
+ as='int((nf+2)/2) * W/nf * 0.29' pd='2*int((nf+1)/2) * (W/nf + 0.29)' ps='2*int((nf+2)/2) * (W/nf + 0.29)'
+ nrd='0.29 / W' nrs='0.29 / W' sa=0 sb=0 sd=0 mult=m_sum m=m_sum
XM23 INC n2 OUTNA vddh2 sky130_fd_pr__pfet_g5v0d10v5 L=l W=wp_sum nf=1 ad='int((nf+1)/2) * W/nf * 0.29'
+ as='int((nf+2)/2) * W/nf * 0.29' pd='2*int((nf+1)/2) * (W/nf + 0.29)' ps='2*int((nf+2)/2) * (W/nf + 0.29)'
+ nrd='0.29 / W' nrs='0.29 / W' sa=0 sb=0 sd=0 mult=m_sum m=m_sum
XM24 OUTPB vgn1 gnd gnd sky130_fd_pr__nfet_g5v0d10v5 L=l W=wn_sum nf=1 ad='int((nf+1)/2) * W/nf * 0.29'
+ as='int((nf+2)/2) * W/nf * 0.29' pd='2*int((nf+1)/2) * (W/nf + 0.29)' ps='2*int((nf+2)/2) * (W/nf + 0.29)'
+ nrd='0.29 / W' nrs='0.29 / W' sa=0 sb=0 sd=0 mult=m_sum m=m_sum
XM25 net33 nn2 OUTPA gnd sky130_fd_pr__nfet_g5v0d10v5 L=l W=wn_sum nf=1 ad='int((nf+1)/2) * W/nf * 0.29'
+ as='int((nf+2)/2) * W/nf * 0.29' pd='2*int((nf+1)/2) * (W/nf + 0.29)' ps='2*int((nf+2)/2) * (W/nf + 0.29)'
+ nrd='0.29 / W' nrs='0.29 / W' sa=0 sb=0 sd=0 mult=m_sum m=m_sum
XM26 OUTPA vgn1 gnd gnd sky130_fd_pr__nfet_g5v0d10v5 L=l W=wn_sum nf=1 ad='int((nf+1)/2) * W/nf * 0.29'
+ as='int((nf+2)/2) * W/nf * 0.29' pd='2*int((nf+1)/2) * (W/nf + 0.29)' ps='2*int((nf+2)/2) * (W/nf + 0.29)'
+ nrd='0.29 / W' nrs='0.29 / W' sa=0 sb=0 sd=0 mult=m_sum m=m_sum
Vmeas20 vddho vddh2 0
.save i(vmeas20)
**** begin user architecture code
.lib $::SKYWATER_MODELS/sky130.lib.spice tt



  .option wnflag=1
  .option safecurrents
  ********************Static Current Sources***************************
  .param base_current=50n
  .param i0=base_current i1={1*i0} i2={2*i0} i3={4*i0} i4={8*i0}
  *Ip0 vddh ip0 i0
  *In0 in0  gnd i0

  *Ip1 vddh ip1 i1
  *In1 in1  gnd i1

  *Ip2 vddh ip2 i2
  *In2 in2  gnd i2

  *Ip3 vddh ip3 i3
  *In3 in3  gnd i3

  *Ip4 vddh ip4 i4
  *In4 in4  gnd i4

  *Ivp vp gnd 0.2u
  *Ivn vddh vn 0.2u
  ********************Static Voltage Sources***************************
  Vddh vddh gnd dc 5.5

  *vb1 vb1 gnd dc 3.2
  *vb2 vb2 gnd dc 2.1

  *vina ina gnd sin({5.5/2} {5.5/2} 100k)
  *vinb inb gnd sin({5.5/2} {-5.5/2} 100k)

  .param vin_val=4.661
  *vin0 in[0] gnd dc vin_val
  *vin1 in[1] gnd dc vin_val
  *vin2 in[2] gnd dc vin_val
  *vin3 in[3] gnd dc vin_val
  *vin4 in[4] gnd dc vin_val
  ********************Dynamic Voltage Sources***************************
  *******Calculation**********
  .param base_f=100e3 base_t={1/base_f} base_th={base_t/2} base_d={base_th}
  .param b0_th={base_th} b0_t={b0_th*2}
  .param b1_th={b0_th*2} b1_t={b1_th*2}
  .param b2_th={b1_th*2} b2_t={b2_th*2}
  .param b3_th={b2_th*2} b3_t={b3_th*2}
  *******Signals**********
  .param vh=1.162 vl=1.044
*  vin0 in[0] gnd dc pulse(5.5 0 {base_d} 1n 1n {b0_th} {b0_t})
  vin0 in[0] gnd dc vl
  Vin1 in[1] gnd pulse({vh} {vl} {base_d} 1n 1n {b0_th} {b0_t})
  Vin2 in[2] gnd pulse({vh} {vl} {base_d} 1n 1n {b1_th} {b1_t})
  Vin3 in[3] gnd pulse({vh} {vl} {base_d} 1n 1n {b2_th} {b2_t})
  Vin4 in[4] gnd pulse({vh} {vl} {base_d} 1n 1n {b3_th} {b3_t})
  ********************Simulation Commands*****************************
  .control
     reset
     save all
     tran 1n 100u
     *dc vin0 -1 6.5 0.01
     *dc R2 1.9meg 2.1meg 10

     *ac dec 100 1 1e9

     let vout_mag =abs(v(out))
     let vout_phase_margin = phase(v(out))*180/pi + 180
     meas ac Aol find vout_mag at = 10
     meas ac UGF when vout_mag=1 fall=1
     meas ac PM find vout_phase_margin when vout_mag=1
     let difference = v(inc) - v(ind)
     save difference
     write op_amp_v2-tb.raw
     wrdata /home/yohanes/10-bit-DAC/simulations/op_amp2-tb.txt out load
     set appendwrite
*    quit 0
  .endc



**** end user architecture code
**.ends
.end
